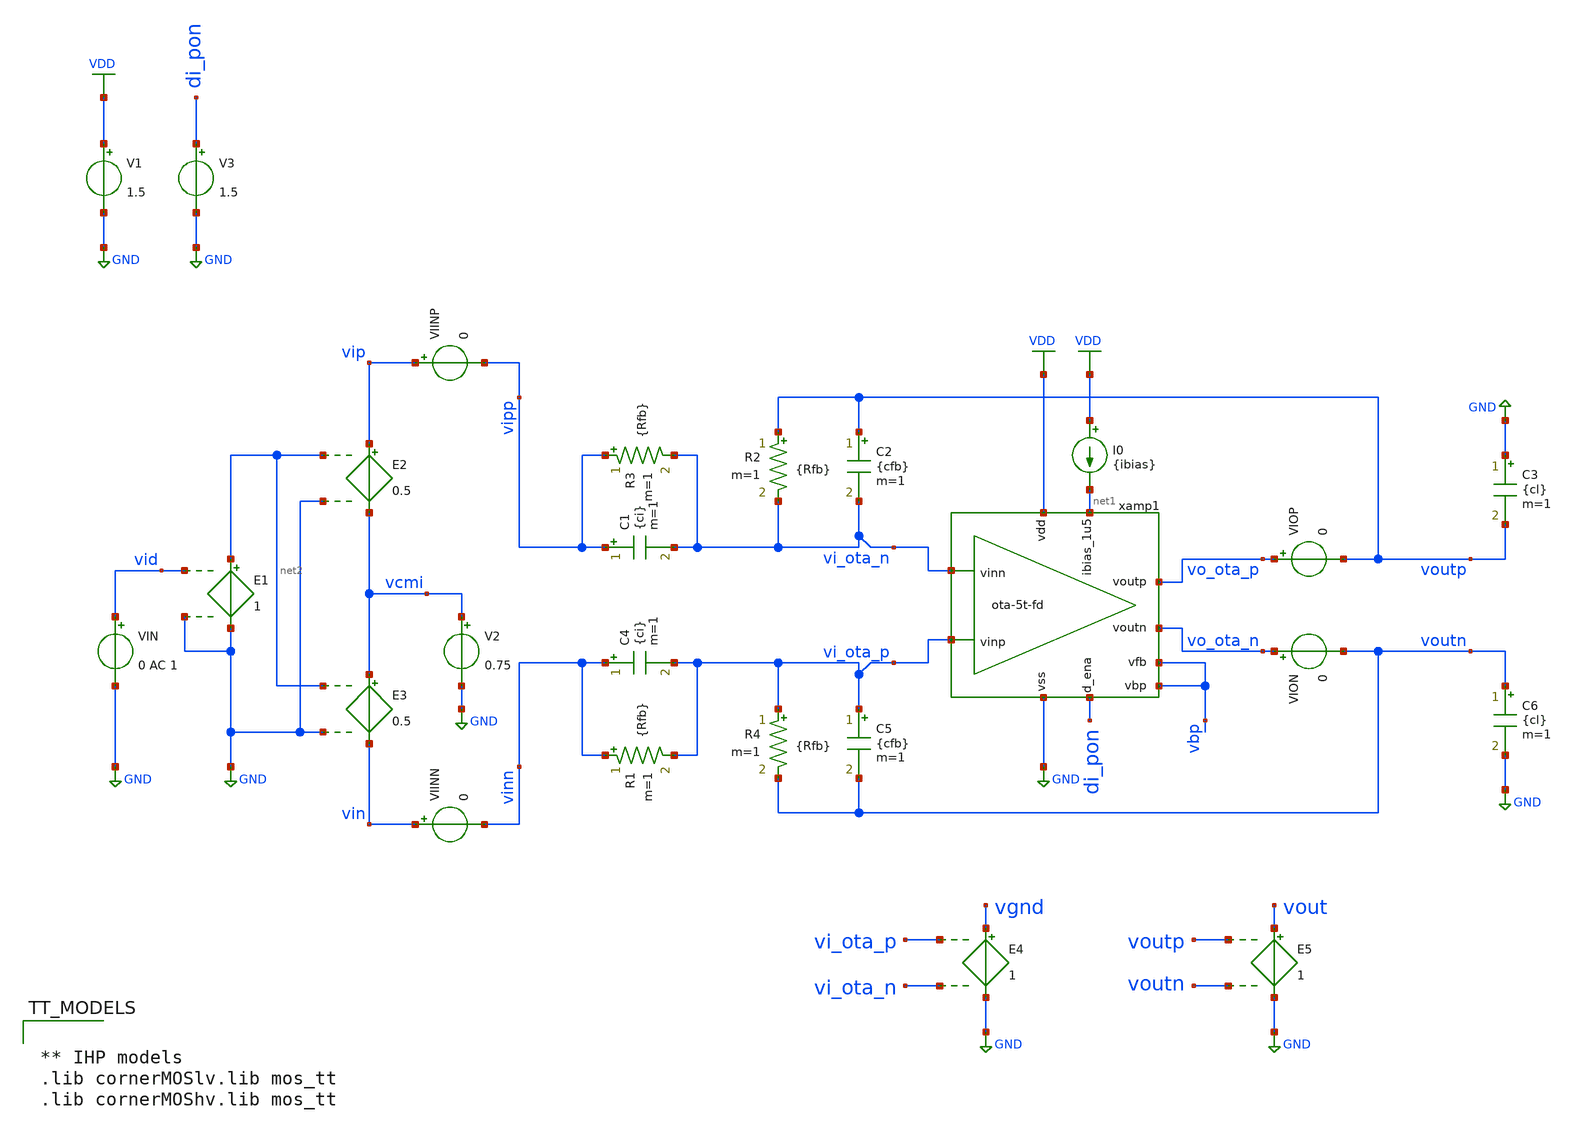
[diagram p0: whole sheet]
** sch_path: xschem/ota-5t-fd_tb-cl.sch
* xschem/ota-5t-fd.sch:
* (c) 2025 M. Koefinger
**.subckt ota-5t-fd_tb-cl
C1 vipp vi_ota_n {ci} m=1
C2 voutp vi_ota_n {cfb} m=1
E5 vout GND voutp voutn 1
VIOP vo_ota_p voutp 0
VION vo_ota_n voutn 0
V1 VDD GND 1.5
V3 di_pon GND 1.5
I0 VDD net1 {ibias}
R2 voutp vi_ota_n {Rfb} m=1
C3 GND voutp {cl} m=1
C4 vinn vi_ota_p {ci} m=1
C5 vi_ota_p voutn {cfb} m=1
C6 voutn GND {cl} m=1
R4 vi_ota_p voutn {Rfb} m=1
xamp1 VDD vbp vo_ota_p vo_ota_n vi_ota_p vi_ota_n net1 di_pon GND vbp ota-5t-fd
R1 vinn vi_ota_p {Rfb} m=1
R3 vipp vi_ota_n {Rfb} m=1
E4 vgnd GND vi_ota_p vi_ota_n 1
V2 vcmi GND 0.75
E3 vcmi vin net2 GND 0.5
E2 vip vcmi net2 GND 0.5
VIN vid GND 0 AC 1
E1 net2 GND vid GND 1
VIINP vip vipp 0
VIINN vin vinn 0
**** begin user architecture code


.include ota-5t-fd_tb-cl.save
*.include ../xschem/ota-5t-fd-dev-sav.spice
.options savecurrents
.options method=gear reltol=.005
.options sparse
.param ibias=20u
.param gain_cl=1
.param ci=100f
.param cfb=ci
.param cl=2*ci
.param Rfb=100M
.param Ri=Rfb
.control
save all

let f_min = 10
let f_max = 1G
let f_stop = 500k

let Adc = 1
let err_gain_spec = 0.004
let v_step_o = 1
let v_step_i = v_step_o/Adc

let t_rf = 0.1u
let t_step = 50uf
let t_delay = 0
let t_per = 2*t_step

let tstep = 0.1*t_rf
let tstop = 2*t_per
let tstart = t_delay

alter @VIN[DC] = 0.0

set wr_singlescale
set wr_vecnames
option numdgt=3

set opSimOnly = 0

** Main Simulations
if $opSimOnly eq 0
	op
	ac dec 100 $&const.f_min $&const.f_max
	noise v(vout) VIN dec 100 $&const.f_min $&const.f_max 1
	noise v(vout) VIN dec 100 100 5Meg
	alter @VIN[PULSE] = [ 0 $&v_step_i $&t_delay $&t_rf $&t_rf $&t_step $&t_per 0 ]
	tran $&tstep $&tstop $&tstart

	setplot ac1
	let A = v(vout)/v(vid)

	let Amag_dB = vdb(A)
	settype decibel Amag_dB
	let Aarg = 180/PI*cphase(A)
	let fdc = const.f_min+1
	meas ac Adc_ol_dB find Amag_dB when frequency = fdc
	let Amag_fc = Adc_ol_dB-3
	meas ac fc find frequency when Amag_dB = Amag_fc
	meas ac Amin min_at Amag_dB from=const.f_min to=fc
	meas ac Amax max Amag_dB
	meas ac Astop find Amag_dB when frequency = const.f_stop
	meas ac fug find frequency when Amag_dB=0
	let err_gain_act = 1-10^(Adc_ol_dB/20)/Adc
	let Adc_ol_min = Adc*(1-err_gain_spec)/err_gain_spec
	let Adc_ol_min_dB = vdb(Adc_ol_min)
	print err_gain_act*100
	print Adc_ol_min_dB
	plot Amag_dB Aarg ylabel 'Magnitude, Phase'

	setplot noise1
	let acgain = onoise_spectrum/inoise_spectrum
	let diffpair = sqrt(2)*onoise_n.xamp1.xmn1.nsg13_lv_nmos
	let load_p = sqrt(2)*onoise_n.xamp1.xmp1.nsg13_lv_pmos
	*plot inoise_spectrum ylog xlog
	plot onoise_spectrum r1 r2 r3 r4 diffpair load_p ylog xlog ylabel 'Output Noise'

	setplot noise4
	let p_noise_q = (1e-3)^2
	let p_noise_o = onoise_total^2
	let p_sig_o = (v_step_o/(2*sqrt(2)))^2
	let snr = p_sig_o/(p_noise_o+p_noise_q)
	let snr_dB = 10*log10(snr)
	print snr_dB
	print onoise_total

	setplot tran4
	let vid = v(vid)
	let iop = viop#branch
	let ion = vion#branch
	let vcmo = (voutp+voutn)/2

	*plot iop ion
	plot vid vout vcmo
	plot v(vip) v(vin) v(voutp) v(voutn) vcmo

end

alter @VIN[DC] = 0
op
remzerovec
write ota-5t-fd_tb-cl.raw
.endc



** IHP models
.lib cornerMOSlv.lib mos_tt
.lib cornerMOShv.lib mos_tt


**** end user architecture code
**.ends

* expanding   symbol:  ota-5t-fd.sym # of pins=10
** sym_path: xschem/ota-5t-fd.sym
** sch_path: xschem/ota-5t-fd.sch
.subckt ota-5t-fd vdd vfb voutp voutn vinp vinn ibias_1u5 d_ena vss vbp
*.ipin ibias_1u5
*.iopin vdd
*.iopin vss
*.ipin vinp
*.ipin vinn
*.opin voutn
*.ipin d_ena
*.opin voutp
*.ipin vfb
*.opin vbp
XMN3 tail gate_n vss vss sg13_lv_nmos w=2.5u l=0.5u ng=5 m=1 mm_ok=1
XMP2 voutp vfb vdd vdd sg13_lv_pmos w=0.5u l=0.5u ng=1 m=1 mm_ok=1
XMN1 voutn vinp tail vss sg13_lv_nmos w=5.5u l=0.5u ng=11 m=1 mm_ok=1
XMN2 voutp vinn tail vss sg13_lv_nmos w=5.5u l=0.5u ng=11 m=1 mm_ok=1
XMP1 voutn vfb vdd vdd sg13_lv_pmos w=0.5u l=0.5u ng=1 m=1 mm_ok=1
XMN4 ibias_1u5 gate_n vss vss sg13_lv_nmos w=1.5u l=0.5u ng=3 m=1 mm_ok=1
XMN5 gate_n ena_n vss vss sg13_lv_nmos w=0.5u l=0.13u ng=1 m=1 mm_ok=1
XMPSW1 vfb ena vdd vdd sg13_lv_pmos w=1.5u l=0.13u ng=1 m=1 mm_ok=1
XMN8 ena ena_n vss vss sg13_lv_nmos w=0.5u l=0.13u ng=1 m=1 mm_ok=1
XMP5 ena ena_n vdd vdd sg13_lv_pmos w=1.5u l=0.13u ng=1 m=1 mm_ok=1
XMN6 ibias_1u5 ena gate_n vss sg13_lv_nmos w=0.5u l=0.13u ng=1 m=1 mm_ok=1
XMN7 ena_n d_ena vss vss sg13_lv_nmos w=0.5u l=0.13u ng=1 m=1 mm_ok=1
XMP4 ena_n d_ena vdd vdd sg13_lv_pmos w=1.5u l=0.13u ng=1 m=1 mm_ok=1
XMN9 vbp gate_n vss vss sg13_lv_nmos w=1u l=0.5u ng=2 m=1 mm_ok=1
XMP3 vbp vbp vdd vdd sg13_lv_pmos w=0.5u l=0.5u ng=1 m=1 mm_ok=1
.ends

.GLOBAL GND
.GLOBAL VDD
.end
